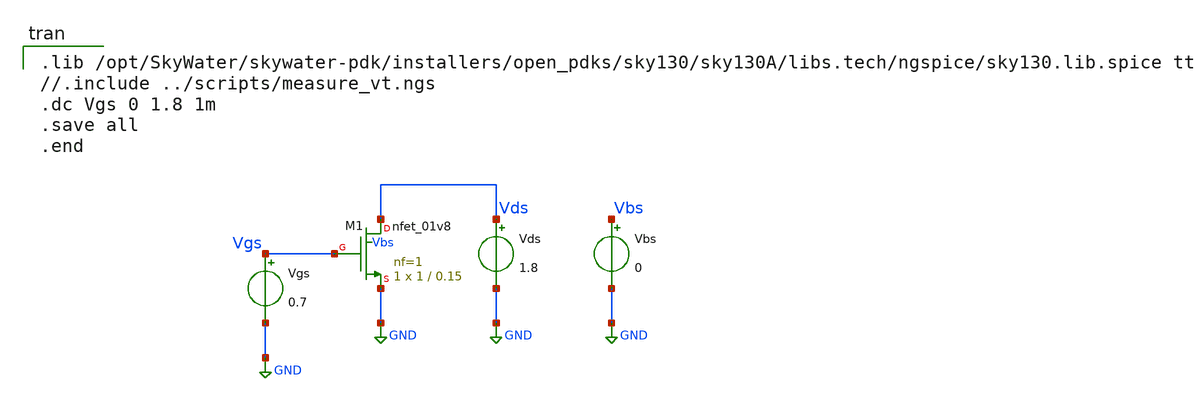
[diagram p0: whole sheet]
** sch_path: 1/xschem/nmos_iv_characteristics.sch
**.subckt nmos_iv_characteristics
XM1 Vds Vgs GND Vbs sky130_fd_pr__nfet_01v8 L=0.15 W=1 nf=1 ad='int((1 + 1)/2) * 1 / 1 * 0.29' as='int((1 + 2)/2) * 1 / 1 * 0.29'
+ pd='2*int((1 + 1)/2) * (1 / 1 + 0.29)' ps='2*int((1 + 2)/2) * (1 / 1 + 0.29)' nrd='0.29 / 1 ' nrs='0.29 / 1 '
+ sa=0 sb=0 sd=0 mult=1 m=1
Vds Vds GND 1.8
.save i(vds)
Vgs Vgs GND 0.7
.save i(vgs)
Vbs Vbs GND 0
.save i(vbs)
**** begin user architecture code

.lib /opt/SkyWater/skywater-pdk/installers/open_pdks/sky130/sky130A/libs.tech/ngspice/sky130.lib.spice tt
//.include ../scripts/measure_vt.ngs
.dc Vgs 0 1.8 1m
.save all
.end

**** end user architecture code
**.ends
.GLOBAL GND
.end
